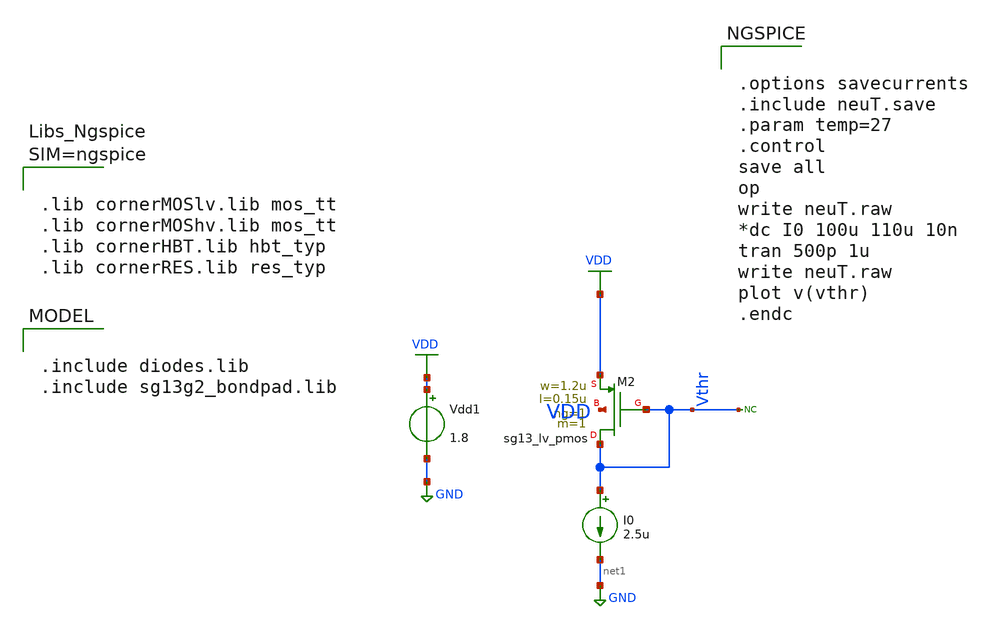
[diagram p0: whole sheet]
** sch_path: blocks/composite/dpi_adexp_neuron/design_data/xschem/neuT.sch
**.subckt neuT
Vdd1 VDD GND 1.8
XM2 Vthr Vthr VDD VDD sg13_lv_pmos w=1.2u l=0.15u ng=1 m=1 mm_ok=1
I0 Vthr net1 2.5u
* noconn Vthr
**** begin user architecture code

.include diodes.lib
.include sg13g2_bondpad.lib



.options savecurrents
.include neuT.save
.param temp=27
.control
save all
op
write neuT.raw
*dc I0 100u 110u 10n
tran 500p 1u
write neuT.raw
plot v(vthr)
.endc





.lib cornerMOSlv.lib mos_tt
.lib cornerMOShv.lib mos_tt
.lib cornerHBT.lib hbt_typ
.lib cornerRES.lib res_typ



**** end user architecture code
**.ends
.GLOBAL GND
.GLOBAL VDD
.end
